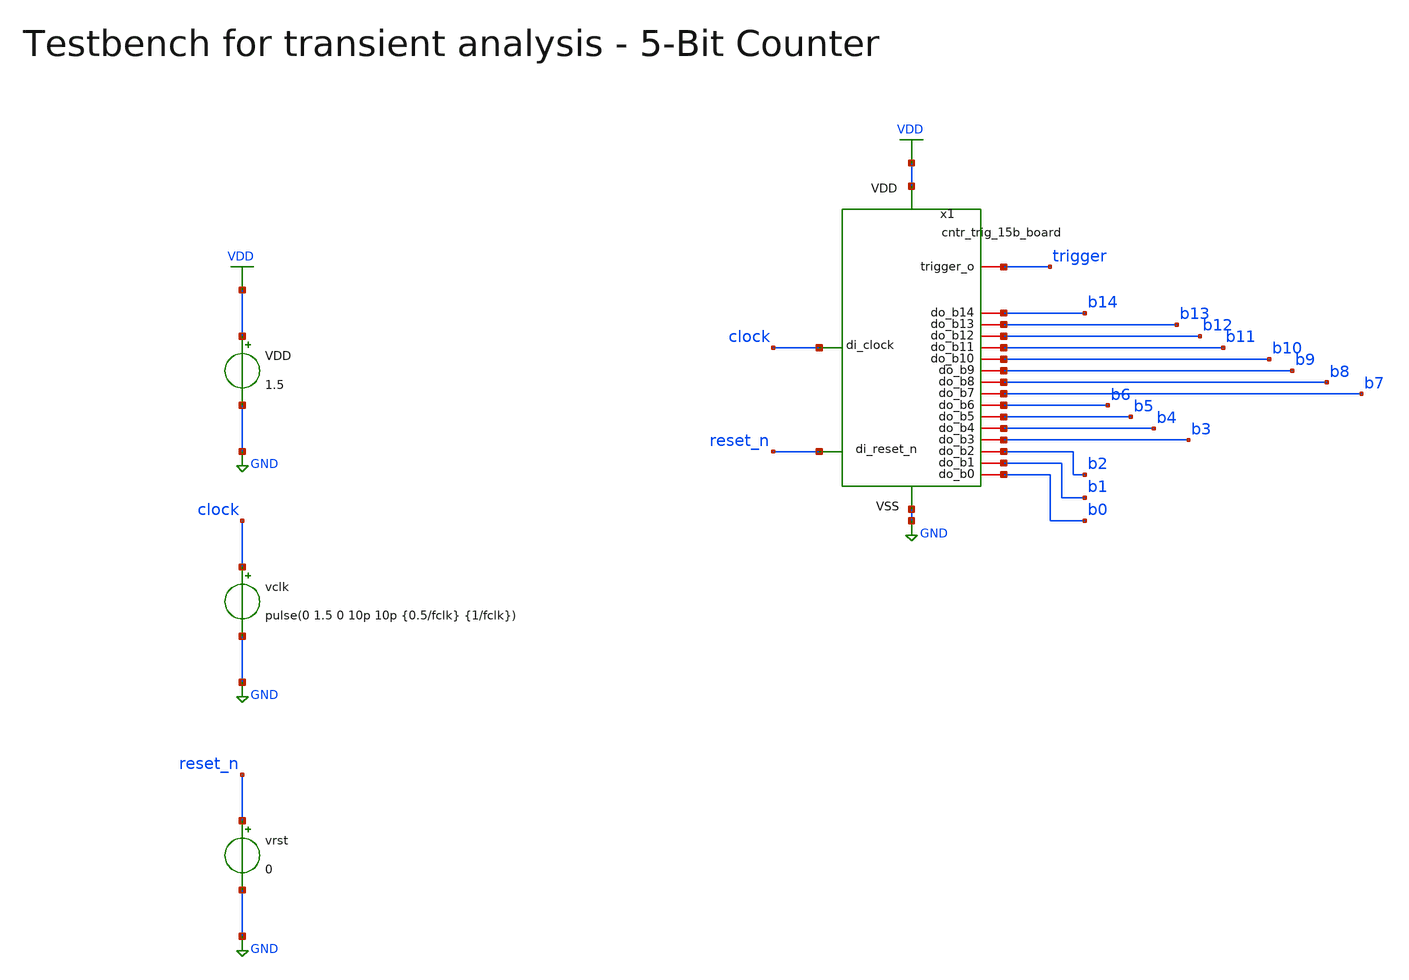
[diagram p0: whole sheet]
** sch_path: xspice/cntr_trig_15b_board_tb_tran.sch
**.subckt cntr_trig_15b_board_tb_tran
VDD VDD GND 1.5
vclk clock GND pulse(0 1.5 0 10p 10p {0.5/fclk} {1/fclk})
vrst reset_n GND 0
x1 VDD GND clock b0 b1 b2 b3 b4 b5 b6 b7 b8 b9 b10 b11 b12 b13 b14 reset_n trigger
+ cntr_trig_15b_board
**** begin user architecture code


*True Mixed Signal Simulation (.xspice)
.include /foss/designs/SG13G2_ASIC-Design-Template/xspice/cntr_trig_15b_board/cntr_trig_15b_board.xspice

.param temp=27
.param fclk=8000000
.options savecurrents
.control
save all

* Transient Analysis
tran 1n 1000u
write cntr_trig_15b_board_tb_tran.raw

plot v(clock) v(enable) v(reset_n)
plot v(b3) v(b2) v(b1) v(b0)

* Writing Data
set wr_singlescale
set wr_vecnames

let clock = clock
let reset_n = reset_n
let b0 = b0
let b1 = b1
let b2 = b2
let b3 = b3
let b4 = b4
let b5 = b5

wrdata
+ /foss/designs/SG13G2_ASIC-Design-Template/python/plot_simulations/data/counter_board_tb_tran.txt clock enable reset_n b0 b1 b2 b3

set appendwrite

* Operating Point Analysis
op
remzerovec
write cntr_trig_15b_board_tb_tran.raw

quit
.endc


.lib cornerMOSlv.lib mos_tt
.lib cornerRES.lib res_typ

**** end user architecture code
**.ends
.GLOBAL GND
.GLOBAL VDD
.end
